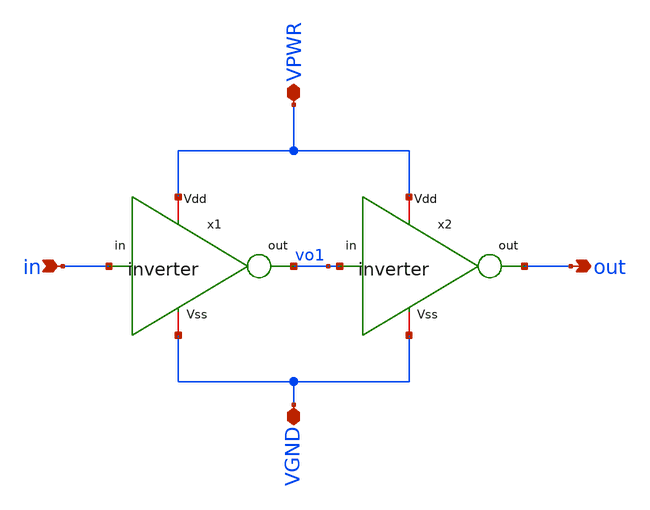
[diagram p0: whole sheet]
** sch_path: Circuits/Buffer/Buffer.sch
**.subckt Buffer in out VPWR VGND
*.ipin in
*.opin out
*.iopin VPWR
*.iopin VGND
x1 VPWR in vo1 VGND inverter
x2 VPWR vo1 out VGND inverter
**.ends

* expanding   symbol:  /home/jakob/Documents/AutomatedLayoutGeneration/Circuits/Buffer/inverter.sym
*+ # of pins=4
** sym_path: Circuits/Buffer/inverter.sym
** sch_path: Circuits/Buffer/inverter.sch
.subckt inverter Vdd in out Vss
*.iopin Vdd
*.iopin Vss
*.ipin in
*.opin out
XM1 out in Vdd Vdd sky130_fd_pr__pfet_01v8 L=0.3 W='1 * 8 ' nf=8 ad='int((nf+1)/2) * W / nf * 0.29' as='int((nf+2)/2) * W / nf * 0.29'
+ pd='2*int((nf+1)/2) * (W / nf + 0.29)' ps='2*int((nf+2)/2) * (W / nf + 0.29)' nrd='0.29 / W ' nrs='0.29 / W '
+ sa=0 sb=0 sd=0 mult=1 m=1
XM2 out in Vss Vss sky130_fd_pr__nfet_01v8 L=0.3 W='1 * 8 ' nf=8 ad='int((nf+1)/2) * W / nf * 0.29' as='int((nf+2)/2) * W / nf * 0.29'
+ pd='2*int((nf+1)/2) * (W / nf + 0.29)' ps='2*int((nf+2)/2) * (W / nf + 0.29)' nrd='0.29 / W ' nrs='0.29 / W '
+ sa=0 sb=0 sd=0 mult=1 m=1
.ends

.end
